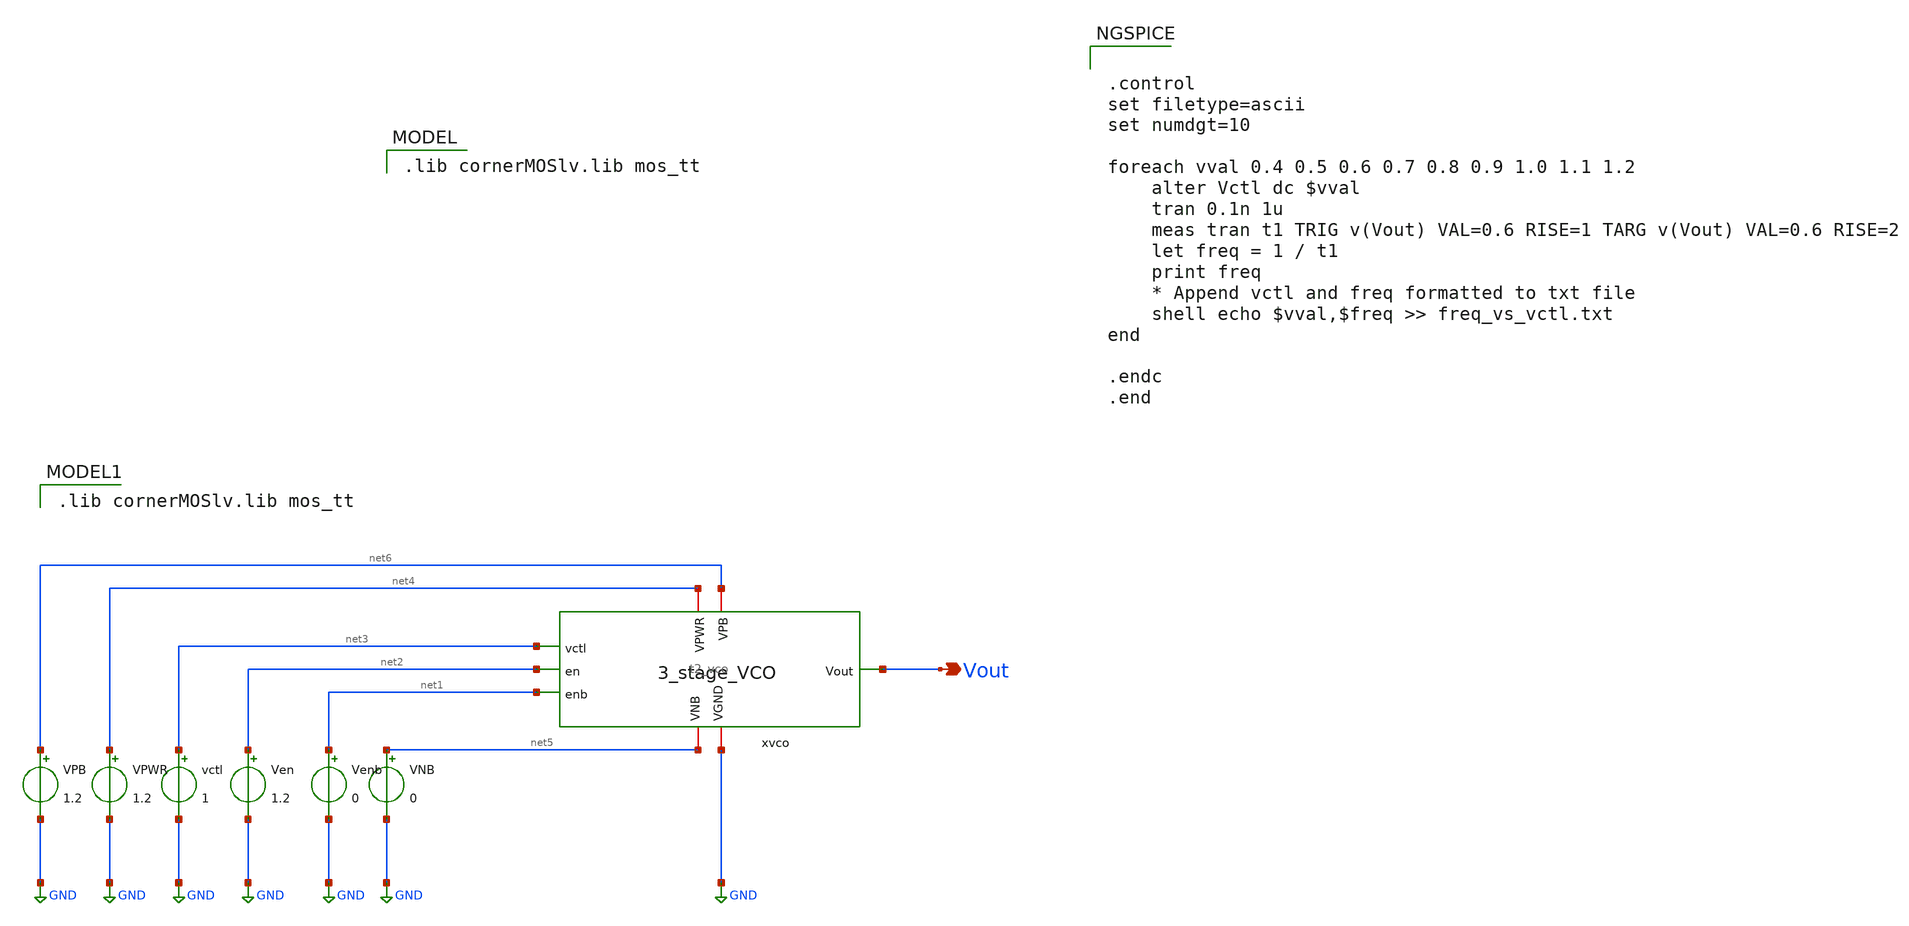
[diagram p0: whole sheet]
** sch_path: Team 2 Design/design_data/xschem/t2_vco_sweep_.sch
**.subckt t2_vco_sweep_ Vout
*.opin Vout
VPWR net4 GND 1.2
vctl net3 GND 1
Ven net2 GND 1.2
Venb net1 GND 0
VNB net5 GND 0
VPB net6 GND 1.2
x1 net4 net6 GND net5 Vout net3 net2 net1 t2_vco
**** begin user architecture code
 .lib cornerMOSlv.lib mos_tt



.control
set filetype=ascii
set numdgt=10

foreach vval 0.4 0.5 0.6 0.7 0.8 0.9 1.0 1.1 1.2
    alter Vctl dc $vval
    tran 0.1n 1u
    meas tran t1 TRIG v(Vout) VAL=0.6 RISE=1 TARG v(Vout) VAL=0.6 RISE=2
    let freq = 1 / t1
    print freq
    * Append vctl and freq formatted to txt file
    shell echo $vval,$freq >> freq_vs_vctl.txt
end

.endc
.end



 .lib cornerMOSlv.lib mos_tt

**** end user architecture code
**.ends
.GLOBAL GND
.end
